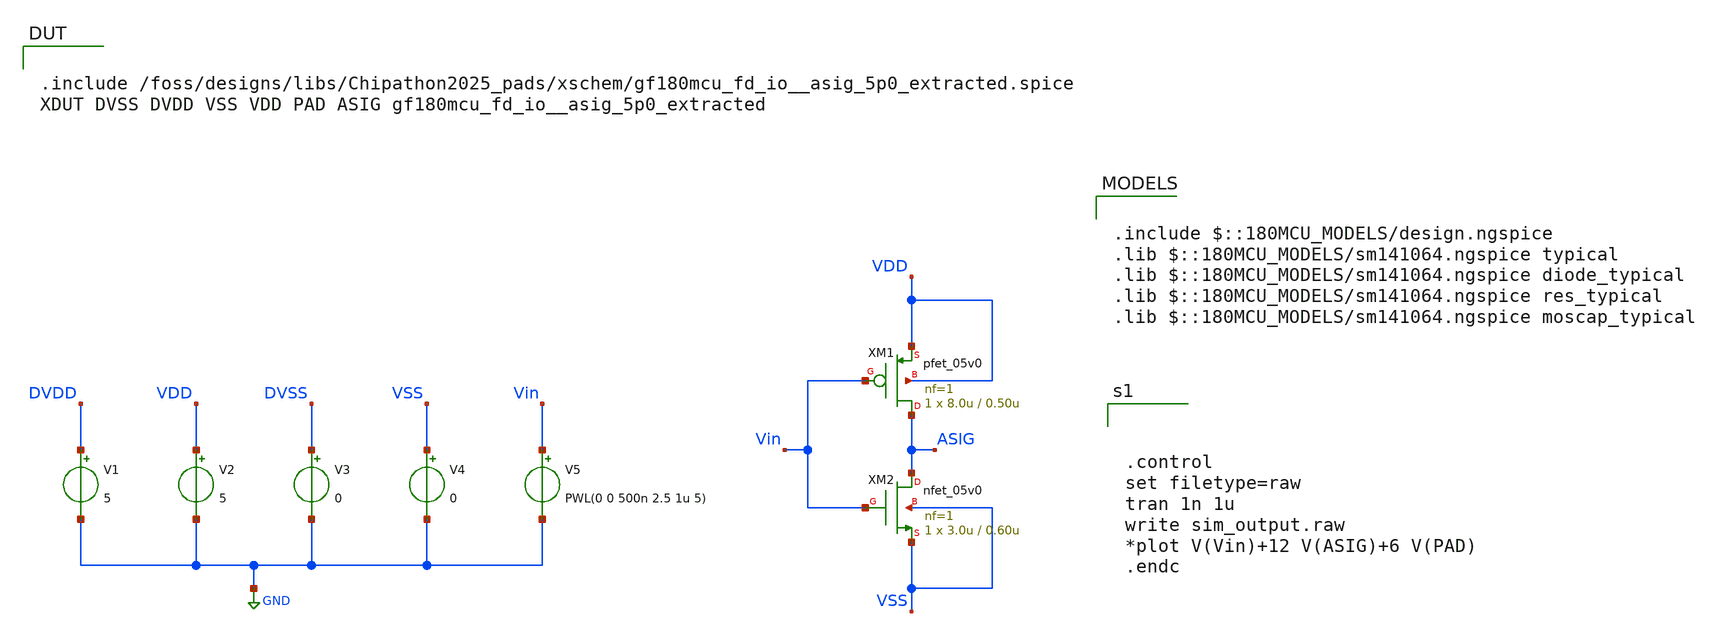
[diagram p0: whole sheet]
** sch_path: designs/libs/Chipathon2025_pads/xschem/asig5V_DC_tb.sch
**.subckt asig5V_DC_tb
V1 DVDD GND 5
V2 VDD GND 5
V3 DVSS GND 0
V4 VSS GND 0
V5 Vin GND PWL(0 0 500n 2.5 1u 5)
XM1 ASIG Vin VDD VDD pfet_05v0 L=0.50u W=8.0u nf=1 ad='int((nf+1)/2) * W/nf * 0.18u' as='int((nf+2)/2) * W/nf * 0.18u'
+ pd='2*int((nf+1)/2) * (W/nf + 0.18u)' ps='2*int((nf+2)/2) * (W/nf + 0.18u)' nrd='0.18u / W' nrs='0.18u / W'
+ sa=0 sb=0 sd=0 m=1
XM2 ASIG Vin VSS VSS nfet_05v0 L=0.60u W=3.0u nf=1 ad='int((nf+1)/2) * W/nf * 0.18u' as='int((nf+2)/2) * W/nf * 0.18u'
+ pd='2*int((nf+1)/2) * (W/nf + 0.18u)' ps='2*int((nf+2)/2) * (W/nf + 0.18u)' nrd='0.18u / W' nrs='0.18u / W'
+ sa=0 sb=0 sd=0 m=1
**** begin user architecture code

.include /foss/designs/libs/Chipathon2025_pads/xschem/gf180mcu_fd_io__asig_5p0_extracted.spice
XDUT DVSS DVDD VSS VDD PAD ASIG gf180mcu_fd_io__asig_5p0_extracted


.include $::180MCU_MODELS/design.ngspice
.lib $::180MCU_MODELS/sm141064.ngspice typical
.lib $::180MCU_MODELS/sm141064.ngspice diode_typical
.lib $::180MCU_MODELS/sm141064.ngspice res_typical
.lib $::180MCU_MODELS/sm141064.ngspice moscap_typical




.control
set filetype=raw
tran 1n 1u
write sim_output.raw
*plot V(Vin)+12 V(ASIG)+6 V(PAD)
.endc


**** end user architecture code
**.ends
.GLOBAL GND
.end
